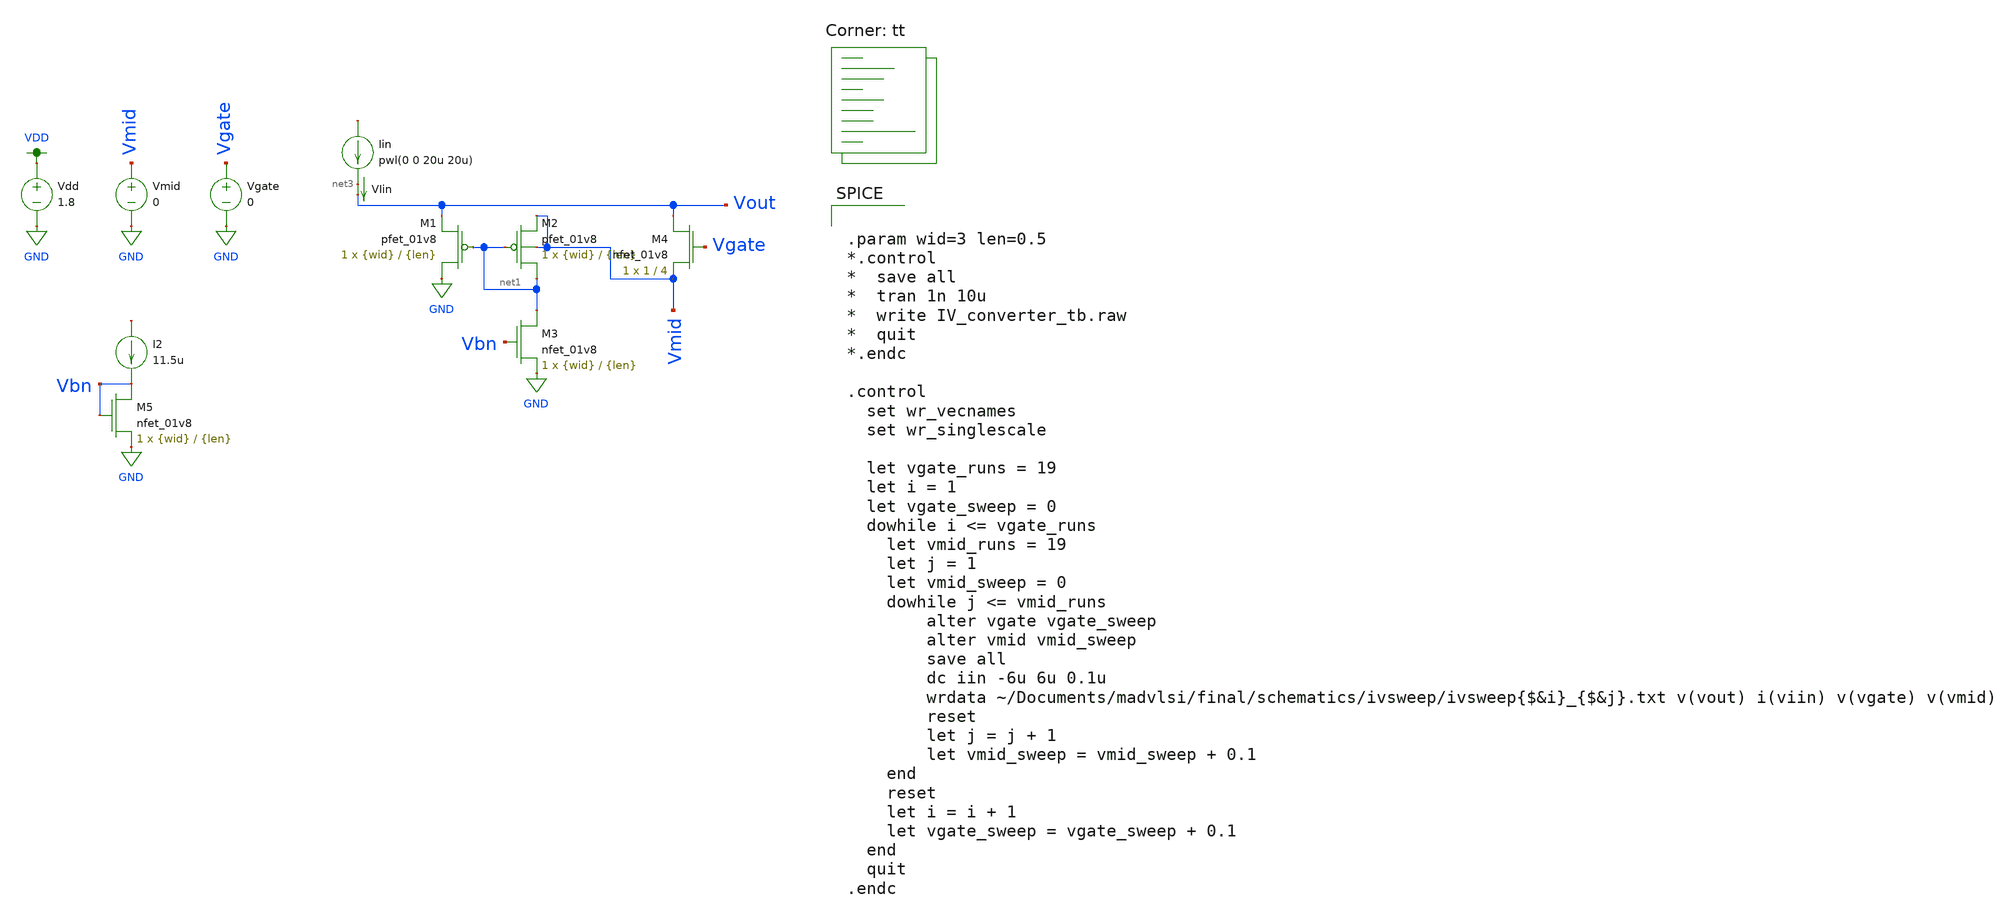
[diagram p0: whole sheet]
** sch_path: final/schematics/IV_converter_tb.sch
**.subckt IV_converter_tb
XM1 GND net1 Vout VDD sky130_fd_pr__pfet_01v8 L={len} W={wid} nf=1 ad='int((nf+1)/2) * W/nf * 0.29' as='int((nf+2)/2) * W/nf * 0.29'
+ pd='2*int((nf+1)/2) * (W/nf + 0.29)' ps='2*int((nf+2)/2) * (W/nf + 0.29)' nrd='0.29 / W' nrs='0.29 / W'
+ sa=0 sb=0 sd=0 mult=1 m=1
XM2 net1 net1 Vmid Vmid sky130_fd_pr__pfet_01v8 L={len} W={wid} nf=1 ad='int((nf+1)/2) * W/nf * 0.29'
+ as='int((nf+2)/2) * W/nf * 0.29' pd='2*int((nf+1)/2) * (W/nf + 0.29)' ps='2*int((nf+2)/2) * (W/nf + 0.29)'
+ nrd='0.29 / W' nrs='0.29 / W' sa=0 sb=0 sd=0 mult=1 m=1
Vdd VDD GND 1.8
Iin net2 net3 pwl(0 0 20u 20u)
I2 net4 Vbn 11.5u
XM5 Vbn Vbn GND GND sky130_fd_pr__nfet_01v8 L={len} W={wid} nf=1 ad='int((nf+1)/2) * W/nf * 0.29' as='int((nf+2)/2) * W/nf * 0.29'
+ pd='2*int((nf+1)/2) * (W/nf + 0.29)' ps='2*int((nf+2)/2) * (W/nf + 0.29)' nrd='0.29 / W' nrs='0.29 / W'
+ sa=0 sb=0 sd=0 mult=1 m=1
Vmid Vmid GND 0
Vgate Vgate GND 0
XM3 net1 Vbn GND GND sky130_fd_pr__nfet_01v8 L={len} W={wid} nf=1 ad='int((nf+1)/2) * W/nf * 0.29' as='int((nf+2)/2) * W/nf * 0.29'
+ pd='2*int((nf+1)/2) * (W/nf + 0.29)' ps='2*int((nf+2)/2) * (W/nf + 0.29)' nrd='0.29 / W' nrs='0.29 / W'
+ sa=0 sb=0 sd=0 mult=1 m=1
XM4 Vout Vgate Vmid GND sky130_fd_pr__nfet_01v8 L=4 W=1 nf=1 ad='int((nf+1)/2) * W/nf * 0.29' as='int((nf+2)/2) * W/nf * 0.29'
+ pd='2*int((nf+1)/2) * (W/nf + 0.29)' ps='2*int((nf+2)/2) * (W/nf + 0.29)' nrd='0.29 / W' nrs='0.29 / W'
+ sa=0 sb=0 sd=0 mult=1 m=1
VIin net3 Vout 0
.save i(viin)
**** begin user architecture code


.param wid=3 len=0.5
*.control
*  save all
*  tran 1n 10u
*  write IV_converter_tb.raw
*  quit
*.endc

.control
  set wr_vecnames
  set wr_singlescale

  let vgate_runs = 19
  let i = 1
  let vgate_sweep = 0
  dowhile i <= vgate_runs
    let vmid_runs = 19
    let j = 1
    let vmid_sweep = 0
    dowhile j <= vmid_runs
        alter vgate vgate_sweep
        alter vmid vmid_sweep
        save all
        dc iin -6u 6u 0.1u
        wrdata ~/Documents/madvlsi/final/schematics/ivsweep/ivsweep{$&i}_{$&j}.txt v(vout) i(viin) v(vgate)
+ v(vmid)
        reset
        let j = j + 1
        let vmid_sweep = vmid_sweep + 0.1
    end
    reset
    let i = i + 1
    let vgate_sweep = vgate_sweep + 0.1
  end
  quit
.endc


.lib $::SKYWATER_MODELS/sky130.lib.spice tt
**** end user architecture code
**.ends
.GLOBAL GND
.GLOBAL VDD
.end
